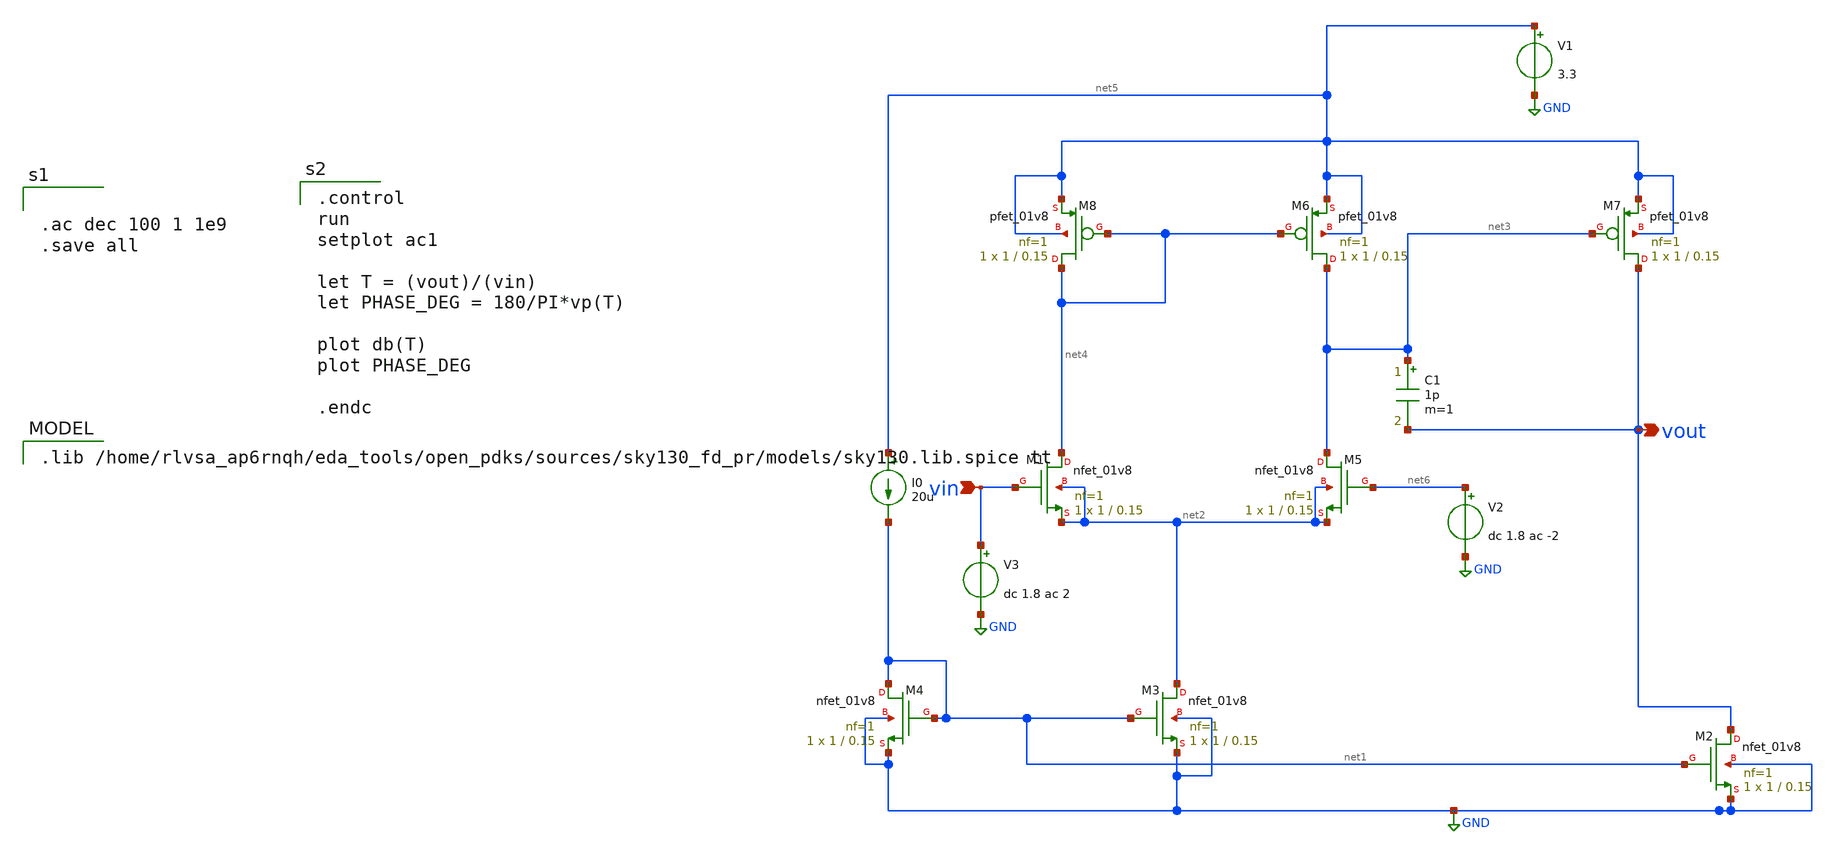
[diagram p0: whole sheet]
** sch_path: Two Stage_Opamp/two_stage_schematic.sch
**.subckt two_stage_schematic vout vin
*.opin vout
*.ipin vin
C1 net3 vout 1p m=1
V1 net5 GND 3.3
V2 net6 GND dc 1.8 ac -2
V3 vin GND dc 1.8 ac 2
I0 net5 net1 20u
XM6 net3 net4 net5 net5 sky130_fd_pr__pfet_01v8 L=0.15 W=1 nf=1 ad='int((1 + 1)/2) * 1 / 1 * 0.29' as='int((1 + 2)/2) * 1 / 1 * 0.29'
+ pd='2*int((1 + 1)/2) * (1 / 1 + 0.29)' ps='2*int((1 + 2)/2) * (1 / 1 + 0.29)' nrd='0.29 / 1 ' nrs='0.29 / 1 '
+ sa=0 sb=0 sd=0 mult=1 m=1
XM7 vout net3 net5 net5 sky130_fd_pr__pfet_01v8 L=0.15 W=1 nf=1 ad='int((1 + 1)/2) * 1 / 1 * 0.29' as='int((1 + 2)/2) * 1 / 1 * 0.29'
+ pd='2*int((1 + 1)/2) * (1 / 1 + 0.29)' ps='2*int((1 + 2)/2) * (1 / 1 + 0.29)' nrd='0.29 / 1 ' nrs='0.29 / 1 '
+ sa=0 sb=0 sd=0 mult=1 m=1
XM8 net4 net4 net5 net5 sky130_fd_pr__pfet_01v8 L=0.15 W=1 nf=1 ad='int((1 + 1)/2) * 1 / 1 * 0.29' as='int((1 + 2)/2) * 1 / 1 * 0.29'
+ pd='2*int((1 + 1)/2) * (1 / 1 + 0.29)' ps='2*int((1 + 2)/2) * (1 / 1 + 0.29)' nrd='0.29 / 1 ' nrs='0.29 / 1 '
+ sa=0 sb=0 sd=0 mult=1 m=1
XM1 net4 vin net2 net2 sky130_fd_pr__nfet_01v8 L=0.15 W=1 nf=1 ad='int((1 + 1)/2) * 1 / 1 * 0.29' as='int((1 + 2)/2) * 1 / 1 * 0.29'
+ pd='2*int((1 + 1)/2) * (1 / 1 + 0.29)' ps='2*int((1 + 2)/2) * (1 / 1 + 0.29)' nrd='0.29 / 1 ' nrs='0.29 / 1 '
+ sa=0 sb=0 sd=0 mult=1 m=1
XM2 vout net1 GND GND sky130_fd_pr__nfet_01v8 L=0.15 W=1 nf=1 ad='int((1 + 1)/2) * 1 / 1 * 0.29' as='int((1 + 2)/2) * 1 / 1 * 0.29'
+ pd='2*int((1 + 1)/2) * (1 / 1 + 0.29)' ps='2*int((1 + 2)/2) * (1 / 1 + 0.29)' nrd='0.29 / 1 ' nrs='0.29 / 1 '
+ sa=0 sb=0 sd=0 mult=1 m=1
XM3 net2 net1 GND GND sky130_fd_pr__nfet_01v8 L=0.15 W=1 nf=1 ad='int((1 + 1)/2) * 1 / 1 * 0.29' as='int((1 + 2)/2) * 1 / 1 * 0.29'
+ pd='2*int((1 + 1)/2) * (1 / 1 + 0.29)' ps='2*int((1 + 2)/2) * (1 / 1 + 0.29)' nrd='0.29 / 1 ' nrs='0.29 / 1 '
+ sa=0 sb=0 sd=0 mult=1 m=1
XM4 net1 net1 GND GND sky130_fd_pr__nfet_01v8 L=0.15 W=1 nf=1 ad='int((1 + 1)/2) * 1 / 1 * 0.29' as='int((1 + 2)/2) * 1 / 1 * 0.29'
+ pd='2*int((1 + 1)/2) * (1 / 1 + 0.29)' ps='2*int((1 + 2)/2) * (1 / 1 + 0.29)' nrd='0.29 / 1 ' nrs='0.29 / 1 '
+ sa=0 sb=0 sd=0 mult=1 m=1
XM5 net3 net6 net2 net2 sky130_fd_pr__nfet_01v8 L=0.15 W=1 nf=1 ad='int((1 + 1)/2) * 1 / 1 * 0.29' as='int((1 + 2)/2) * 1 / 1 * 0.29'
+ pd='2*int((1 + 1)/2) * (1 / 1 + 0.29)' ps='2*int((1 + 2)/2) * (1 / 1 + 0.29)' nrd='0.29 / 1 ' nrs='0.29 / 1 '
+ sa=0 sb=0 sd=0 mult=1 m=1
**** begin user architecture code


.ac dec 100 1 1e9
.save all


.lib /home/rlvsa_ap6rnqh/eda_tools/open_pdks/sources/sky130_fd_pr/models/sky130.lib.spice tt


.control
run
setplot ac1

let T = (vout)/(vin)
let PHASE_DEG = 180/PI*vp(T)

plot db(T)
plot PHASE_DEG

.endc

**** end user architecture code
**.ends
.GLOBAL GND
.end
